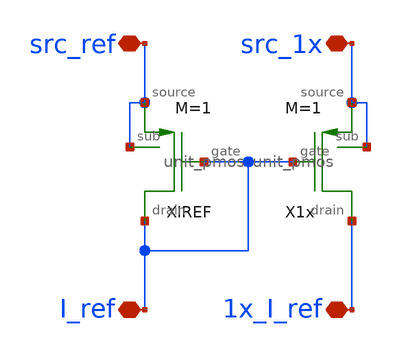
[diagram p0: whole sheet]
** sch_path: designs/libs/core_current_mirror/pmos_current_mirror_sources_io/pmos_current_mirror_sources_io.sch
**.subckt pmos_current_mirror_sources_io I_ref src_ref 1x_I_ref src_1x
*.iopin I_ref
*.iopin src_ref
*.iopin 1x_I_ref
*.iopin src_1x
XIREF I_ref src_ref I_ref src_ref unit_pmos M=1
X1x 1x_I_ref src_1x I_ref src_1x unit_pmos M=1
**.ends

* expanding   symbol:  libs/core_single_mos/unit_pmos/unit_pmos.sym # of pins=4
** sym_path: designs/libs/core_single_mos/unit_pmos/unit_pmos.sym
** sch_path: designs/libs/core_single_mos/unit_pmos/unit_pmos.sch
.subckt unit_pmos drain sub gate source
*.iopin drain
*.iopin source
*.iopin sub
*.iopin gate
**** begin user architecture code

.param M=1

**** end user architecture code
XM1 drain gate source sub pfet_03v3 L=0.5u W=48u nf=8 ad='int((nf+1)/2) * W/nf * 0.18u' as='int((nf+2)/2) * W/nf * 0.18u'
+ pd='2*int((nf+1)/2) * (W/nf + 0.18u)' ps='2*int((nf+2)/2) * (W/nf + 0.18u)' nrd='0.18u / W' nrs='0.18u / W'
+ sa=0 sb=0 sd=0 m={M}
.ends

.end
